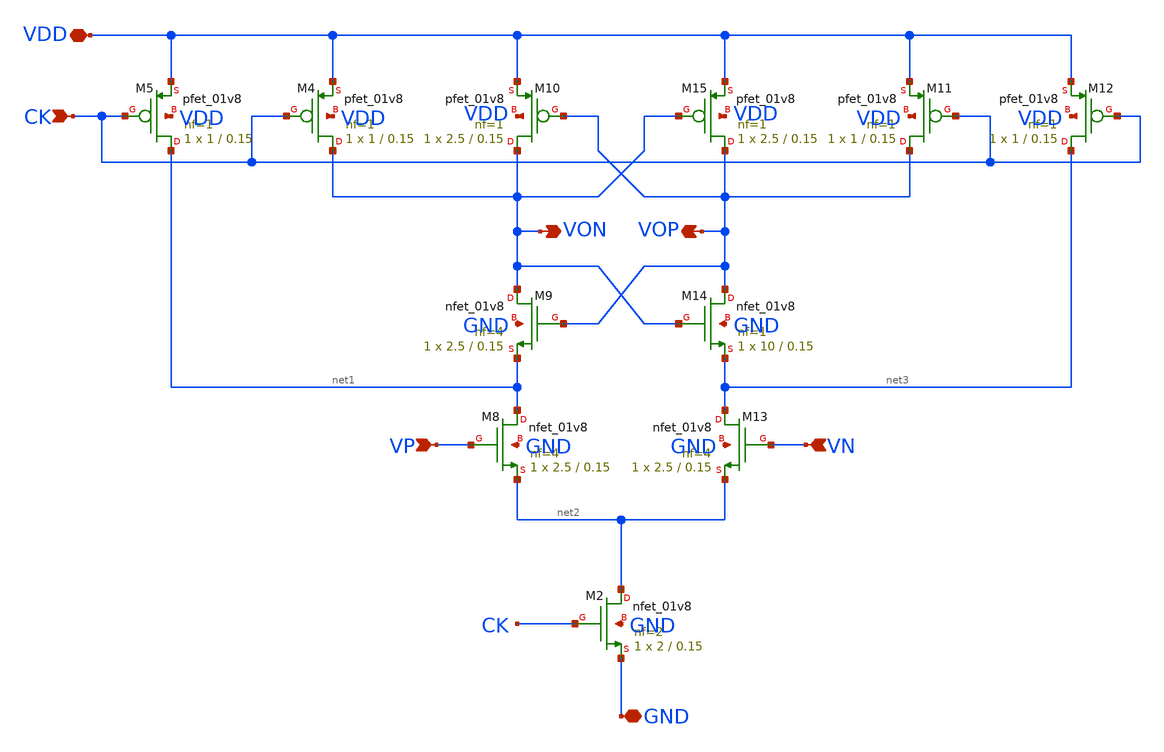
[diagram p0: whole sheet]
** sch_path: xschem/comparator/strongarm.sch
**.subckt strongarm GND VP VOP VON VN VDD CK
*.iopin GND
*.ipin VP
*.opin VOP
*.opin VON
*.ipin VN
*.iopin VDD
*.ipin CK
XM2 net2 CK GND GND sky130_fd_pr__nfet_01v8 L=0.15 W=2 nf=2 ad='int((nf+1)/2) * W/nf * 0.29' as='int((nf+2)/2) * W/nf * 0.29'
+ pd='2*int((nf+1)/2) * (W/nf + 0.29)' ps='2*int((nf+2)/2) * (W/nf + 0.29)' nrd='0.29 / W' nrs='0.29 / W'
+ sa=0 sb=0 sd=0 mult=1 m=1
XM4 VON CK VDD VDD sky130_fd_pr__pfet_01v8 L=0.15 W=1 nf=1 ad='int((nf+1)/2) * W/nf * 0.29' as='int((nf+2)/2) * W/nf * 0.29'
+ pd='2*int((nf+1)/2) * (W/nf + 0.29)' ps='2*int((nf+2)/2) * (W/nf + 0.29)' nrd='0.29 / W' nrs='0.29 / W'
+ sa=0 sb=0 sd=0 mult=1 m=1
XM5 net1 CK VDD VDD sky130_fd_pr__pfet_01v8 L=0.15 W=1 nf=1 ad='int((nf+1)/2) * W/nf * 0.29' as='int((nf+2)/2) * W/nf * 0.29'
+ pd='2*int((nf+1)/2) * (W/nf + 0.29)' ps='2*int((nf+2)/2) * (W/nf + 0.29)' nrd='0.29 / W' nrs='0.29 / W'
+ sa=0 sb=0 sd=0 mult=1 m=1
XM8 net1 VP net2 GND sky130_fd_pr__nfet_01v8 L=0.15 W=2.5 nf=4 ad='int((nf+1)/2) * W/nf * 0.29' as='int((nf+2)/2) * W/nf * 0.29'
+ pd='2*int((nf+1)/2) * (W/nf + 0.29)' ps='2*int((nf+2)/2) * (W/nf + 0.29)' nrd='0.29 / W' nrs='0.29 / W'
+ sa=0 sb=0 sd=0 mult=1 m=1
XM9 VON VOP net1 GND sky130_fd_pr__nfet_01v8 L=0.15 W=2.5 nf=4 ad='int((nf+1)/2) * W/nf * 0.29' as='int((nf+2)/2) * W/nf * 0.29'
+ pd='2*int((nf+1)/2) * (W/nf + 0.29)' ps='2*int((nf+2)/2) * (W/nf + 0.29)' nrd='0.29 / W' nrs='0.29 / W'
+ sa=0 sb=0 sd=0 mult=1 m=1
XM10 VON VOP VDD VDD sky130_fd_pr__pfet_01v8 L=0.15 W=2.5 nf=1 ad='int((nf+1)/2) * W/nf * 0.29' as='int((nf+2)/2) * W/nf * 0.29'
+ pd='2*int((nf+1)/2) * (W/nf + 0.29)' ps='2*int((nf+2)/2) * (W/nf + 0.29)' nrd='0.29 / W' nrs='0.29 / W'
+ sa=0 sb=0 sd=0 mult=1 m=1
XM11 VOP CK VDD VDD sky130_fd_pr__pfet_01v8 L=0.15 W=1 nf=1 ad='int((nf+1)/2) * W/nf * 0.29' as='int((nf+2)/2) * W/nf * 0.29'
+ pd='2*int((nf+1)/2) * (W/nf + 0.29)' ps='2*int((nf+2)/2) * (W/nf + 0.29)' nrd='0.29 / W' nrs='0.29 / W'
+ sa=0 sb=0 sd=0 mult=1 m=1
XM12 net3 CK VDD VDD sky130_fd_pr__pfet_01v8 L=0.15 W=1 nf=1 ad='int((nf+1)/2) * W/nf * 0.29' as='int((nf+2)/2) * W/nf * 0.29'
+ pd='2*int((nf+1)/2) * (W/nf + 0.29)' ps='2*int((nf+2)/2) * (W/nf + 0.29)' nrd='0.29 / W' nrs='0.29 / W'
+ sa=0 sb=0 sd=0 mult=1 m=1
XM13 net3 VN net2 GND sky130_fd_pr__nfet_01v8 L=0.15 W=2.5 nf=4 ad='int((nf+1)/2) * W/nf * 0.29' as='int((nf+2)/2) * W/nf * 0.29'
+ pd='2*int((nf+1)/2) * (W/nf + 0.29)' ps='2*int((nf+2)/2) * (W/nf + 0.29)' nrd='0.29 / W' nrs='0.29 / W'
+ sa=0 sb=0 sd=0 mult=1 m=1
XM14 VOP VON net3 GND sky130_fd_pr__nfet_01v8 L=0.15 W=10 nf=1 ad='int((nf+1)/2) * W/nf * 0.29' as='int((nf+2)/2) * W/nf * 0.29'
+ pd='2*int((nf+1)/2) * (W/nf + 0.29)' ps='2*int((nf+2)/2) * (W/nf + 0.29)' nrd='0.29 / W' nrs='0.29 / W'
+ sa=0 sb=0 sd=0 mult=1 m=1
XM15 VOP VON VDD VDD sky130_fd_pr__pfet_01v8 L=0.15 W=2.5 nf=1 ad='int((nf+1)/2) * W/nf * 0.29' as='int((nf+2)/2) * W/nf * 0.29'
+ pd='2*int((nf+1)/2) * (W/nf + 0.29)' ps='2*int((nf+2)/2) * (W/nf + 0.29)' nrd='0.29 / W' nrs='0.29 / W'
+ sa=0 sb=0 sd=0 mult=1 m=1
**.ends
.end
